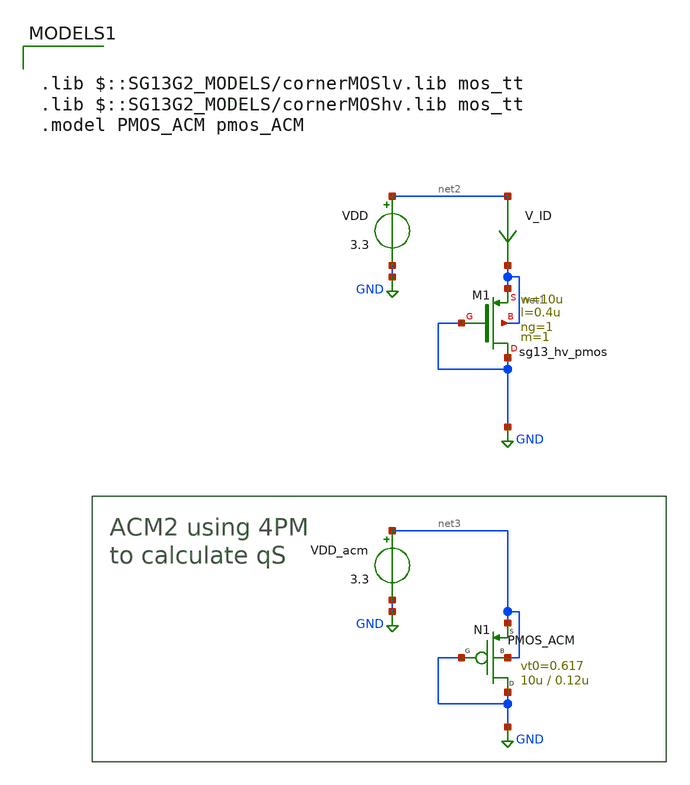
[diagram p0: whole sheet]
** sch_path: legacy/Examples/IHP-SG13/xschem/Extraction/pmos_zeta.sch
**.subckt pmos_zeta
VDD net2 GND 3.3
V_ID net2 net1 0
.save i(v_id)
VDD_acm net3 GND 3.3
N1 GND GND net3 net3 PMOS_ACM w=10u l=0.12u n=1.47 is=0.67u vt0=0.617 sigma=9m zeta=1p
XM1 GND GND net1 net1 sg13_hv_pmos w=10u l=0.4u ng=1 m=1 mm_ok=1
**** begin user architecture code



.control
pre_osdi ./PMOS_ACM_2V0.osdi
pre_osdi ./psp103_nqs.osdi
save all

op

let IDsat_=i(V_ID)
save IDsat_

let IS=@n1[is]
save IS

let qS=@n1[qS_op]
save qS

let idsat=IDsat_/IS
save idsat

let sqr=sqrt(1+idsat)
save sqr

let aux1 = 2*(qS+1-sqr)
save aux1

let zeta = aux1/idsat
save zeta

set appenwrite
write pmos_zeta.raw


.endc



.lib $::SG13G2_MODELS/cornerMOSlv.lib mos_tt
.lib $::SG13G2_MODELS/cornerMOShv.lib mos_tt
.model PMOS_ACM pmos_ACM

**** end user architecture code
**.ends
.GLOBAL GND
.end
